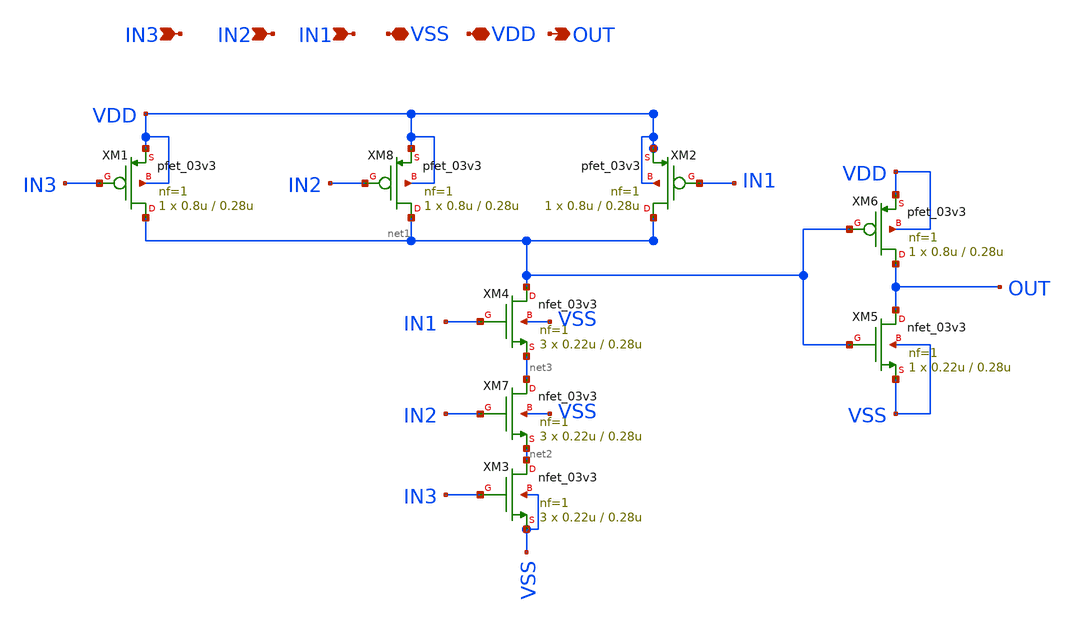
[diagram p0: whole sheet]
** sch_path: Clock_Generator_PAKISTAN_02/Schematics/and_3.sch
**.subckt and_3 IN2 IN1 VSS VDD OUT IN3
*.ipin IN2
*.ipin IN1
*.iopin VSS
*.iopin VDD
*.opin OUT
*.ipin IN3
XM3 net2 IN3 VSS VSS nfet_03v3 L=0.28u W=0.22u nf=1 ad='int((nf+1)/2) * W/nf * 0.18u' as='int((nf+2)/2) * W/nf * 0.18u'
+ pd='2*int((nf+1)/2) * (W/nf + 0.18u)' ps='2*int((nf+2)/2) * (W/nf + 0.18u)' nrd='0.18u / W' nrs='0.18u / W'
+ sa=0 sb=0 sd=0 m=3
XM4 net1 IN1 net3 VSS nfet_03v3 L=0.28u W=0.22u nf=1 ad='int((nf+1)/2) * W/nf * 0.18u' as='int((nf+2)/2) * W/nf * 0.18u'
+ pd='2*int((nf+1)/2) * (W/nf + 0.18u)' ps='2*int((nf+2)/2) * (W/nf + 0.18u)' nrd='0.18u / W' nrs='0.18u / W'
+ sa=0 sb=0 sd=0 m=3
XM5 OUT net1 VSS VSS nfet_03v3 L=0.28u W=0.22u nf=1 ad='int((nf+1)/2) * W/nf * 0.18u' as='int((nf+2)/2) * W/nf * 0.18u'
+ pd='2*int((nf+1)/2) * (W/nf + 0.18u)' ps='2*int((nf+2)/2) * (W/nf + 0.18u)' nrd='0.18u / W' nrs='0.18u / W'
+ sa=0 sb=0 sd=0 m=1
XM6 OUT net1 VDD VDD pfet_03v3 L=0.28u W=0.8u nf=1 ad='int((nf+1)/2) * W/nf * 0.18u' as='int((nf+2)/2) * W/nf * 0.18u'
+ pd='2*int((nf+1)/2) * (W/nf + 0.18u)' ps='2*int((nf+2)/2) * (W/nf + 0.18u)' nrd='0.18u / W' nrs='0.18u / W'
+ sa=0 sb=0 sd=0 m=1
XM1 net1 IN3 VDD VDD pfet_03v3 L=0.28u W=0.8u nf=1 ad='int((nf+1)/2) * W/nf * 0.18u' as='int((nf+2)/2) * W/nf * 0.18u'
+ pd='2*int((nf+1)/2) * (W/nf + 0.18u)' ps='2*int((nf+2)/2) * (W/nf + 0.18u)' nrd='0.18u / W' nrs='0.18u / W'
+ sa=0 sb=0 sd=0 m=1
XM2 net1 IN1 VDD VDD pfet_03v3 L=0.28u W=0.8u nf=1 ad='int((nf+1)/2) * W/nf * 0.18u' as='int((nf+2)/2) * W/nf * 0.18u'
+ pd='2*int((nf+1)/2) * (W/nf + 0.18u)' ps='2*int((nf+2)/2) * (W/nf + 0.18u)' nrd='0.18u / W' nrs='0.18u / W'
+ sa=0 sb=0 sd=0 m=1
XM7 net3 IN2 net2 VSS nfet_03v3 L=0.28u W=0.22u nf=1 ad='int((nf+1)/2) * W/nf * 0.18u' as='int((nf+2)/2) * W/nf * 0.18u'
+ pd='2*int((nf+1)/2) * (W/nf + 0.18u)' ps='2*int((nf+2)/2) * (W/nf + 0.18u)' nrd='0.18u / W' nrs='0.18u / W'
+ sa=0 sb=0 sd=0 m=3
XM8 net1 IN2 VDD VDD pfet_03v3 L=0.28u W=0.8u nf=1 ad='int((nf+1)/2) * W/nf * 0.18u' as='int((nf+2)/2) * W/nf * 0.18u'
+ pd='2*int((nf+1)/2) * (W/nf + 0.18u)' ps='2*int((nf+2)/2) * (W/nf + 0.18u)' nrd='0.18u / W' nrs='0.18u / W'
+ sa=0 sb=0 sd=0 m=1
**.ends
.end
